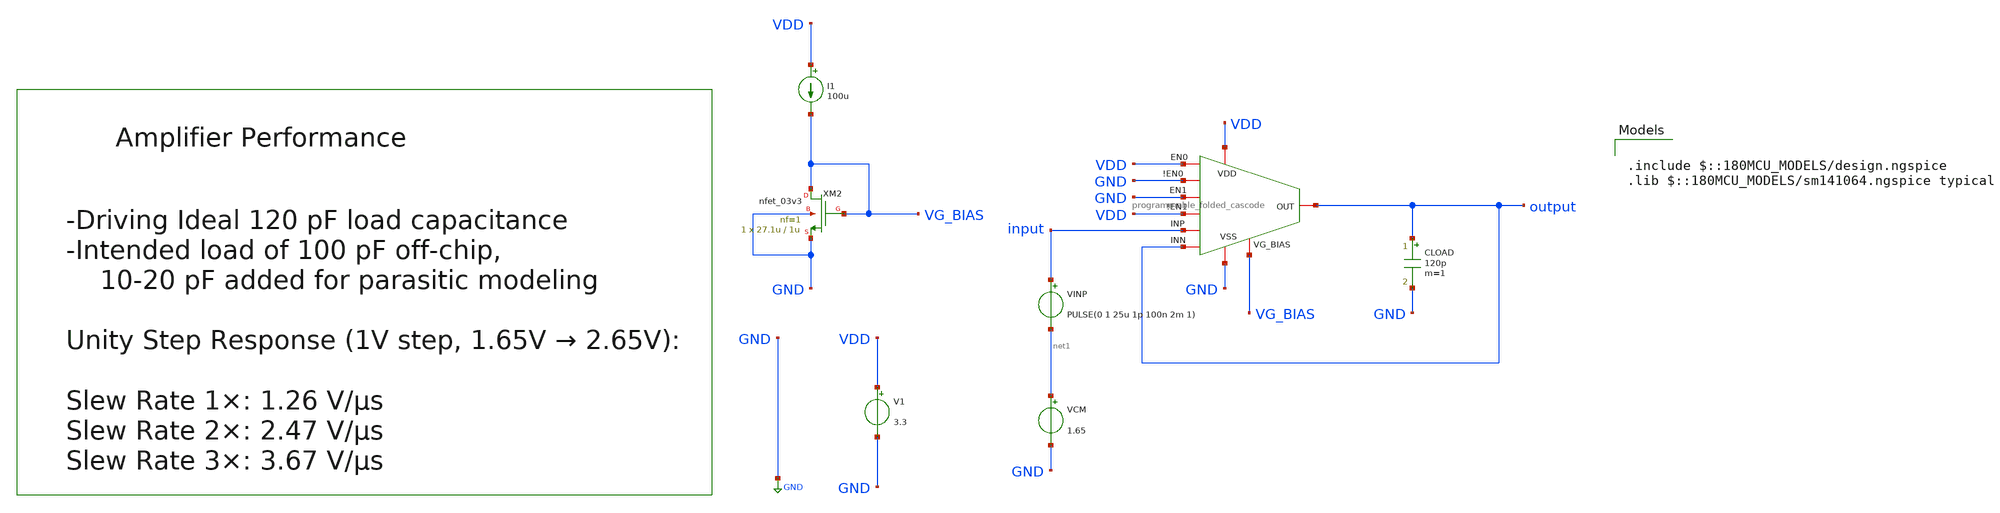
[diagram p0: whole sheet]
** sch_path: designs/libs/core_amps/ota_folded_cascode/prgram_tb/unity_step_tran_SR_tb.sch
**.subckt unity_step_tran_SR_tb
CLOAD output GND 120p m=1
VINP input net1 PULSE(0 1 25u 1p 100n 2m 1)
VCM net1 GND 1.65
x1 VDD VDD GND GND GND VDD output input output VG_BIAS programmable_folded_cascode
XM2 VG_BIAS VG_BIAS GND GND nfet_03v3 L=1u W=27.1u nf=1 ad='int((nf+1)/2) * W/nf * 0.18u' as='int((nf+2)/2) * W/nf * 0.18u'
+ pd='2*int((nf+1)/2) * (W/nf + 0.18u)' ps='2*int((nf+2)/2) * (W/nf + 0.18u)' nrd='0.18u / W' nrs='0.18u / W'
+ sa=0 sb=0 sd=0 m=1
I1 VDD VG_BIAS 100u
V1 VDD GND 3.3
**** begin user architecture code

.include $::180MCU_MODELS/design.ngspice
.lib $::180MCU_MODELS/sm141064.ngspice typical



.control
tran 1n 100u
meas tran v_before find v(output) at=24u
meas tran v_after find v(output) at=90u
let v_20 = v_before + 0.2 * (v_after - v_before)
let v_80 = v_before + 0.8 * (v_after - v_before)
meas tran t_20 when v(output) = v_20 rise = 1 from = 25u
meas tran t_80 when v(output) = v_80 rise = 1 from = 25u
let slew_rate = (v_80 - v_20) / (t_80 - t_20)
print v_before v_after
print slew_rate

plot v(input) v(output)
.endc



**** end user architecture code
**.ends

* expanding   symbol:  libs/core_amps/ota_folded_cascode/prgrm_schem/programmable_folded_cascode.sym
*+ # of pins=10
** sym_path: designs/libs/core_amps/ota_folded_cascode/prgrm_schem/programmable_folded_cascode.sym
** sch_path: designs/libs/core_amps/ota_folded_cascode/prgrm_schem/programmable_folded_cascode.sch
.subckt programmable_folded_cascode EN0 VDD !EN0 VSS EN1 !EN1 INN INP OUT VG_BIAS
*.iopin OUT
*.iopin VSS
*.iopin VDD
*.iopin EN0
*.iopin !EN0
*.iopin EN1
*.iopin !EN1
*.iopin INN
*.iopin INP
*.iopin VG_BIAS
XM29 net7 net7 VDD VDD pfet_03v3 L=1u W=23u nf=1 ad='int((nf+1)/2) * W/nf * 0.18u' as='int((nf+2)/2) * W/nf * 0.18u'
+ pd='2*int((nf+1)/2) * (W/nf + 0.18u)' ps='2*int((nf+2)/2) * (W/nf + 0.18u)' nrd='0.18u / W' nrs='0.18u / W'
+ sa=0 sb=0 sd=0 m=5
XM30 VBP2 VBP2 net7 VDD pfet_03v3 L=.5u W=19.6u nf=1 ad='int((nf+1)/2) * W/nf * 0.18u' as='int((nf+2)/2) * W/nf * 0.18u'
+ pd='2*int((nf+1)/2) * (W/nf + 0.18u)' ps='2*int((nf+2)/2) * (W/nf + 0.18u)' nrd='0.18u / W' nrs='0.18u / W'
+ sa=0 sb=0 sd=0 m=10
XM31 VBP2 VG_BIAS VSS VSS nfet_03v3 L=1u W=27.1u nf=1 ad='int((nf+1)/2) * W/nf * 0.18u' as='int((nf+2)/2) * W/nf * 0.18u'
+ pd='2*int((nf+1)/2) * (W/nf + 0.18u)' ps='2*int((nf+2)/2) * (W/nf + 0.18u)' nrd='0.18u / W' nrs='0.18u / W'
+ sa=0 sb=0 sd=0 m=1
XM32 VBN1 VBN1 VSS VSS nfet_03v3 L=1u W=27.1u nf=1 ad='int((nf+1)/2) * W/nf * 0.18u' as='int((nf+2)/2) * W/nf * 0.18u'
+ pd='2*int((nf+1)/2) * (W/nf + 0.18u)' ps='2*int((nf+2)/2) * (W/nf + 0.18u)' nrd='0.18u / W' nrs='0.18u / W'
+ sa=0 sb=0 sd=0 m=1
XM33 VBN1 net7 VDD VDD pfet_03v3 L=1u W=23u nf=1 ad='int((nf+1)/2) * W/nf * 0.18u' as='int((nf+2)/2) * W/nf * 0.18u'
+ pd='2*int((nf+1)/2) * (W/nf + 0.18u)' ps='2*int((nf+2)/2) * (W/nf + 0.18u)' nrd='0.18u / W' nrs='0.18u / W'
+ sa=0 sb=0 sd=0 m=5
XM34 VBP1 VBP1 VDD VDD pfet_03v3 L=1u W=23u nf=1 ad='int((nf+1)/2) * W/nf * 0.18u' as='int((nf+2)/2) * W/nf * 0.18u'
+ pd='2*int((nf+1)/2) * (W/nf + 0.18u)' ps='2*int((nf+2)/2) * (W/nf + 0.18u)' nrd='0.18u / W' nrs='0.18u / W'
+ sa=0 sb=0 sd=0 m=5
XM35 VBP1 VG_BIAS VSS VSS nfet_03v3 L=1u W=27.1u nf=1 ad='int((nf+1)/2) * W/nf * 0.18u' as='int((nf+2)/2) * W/nf * 0.18u'
+ pd='2*int((nf+1)/2) * (W/nf + 0.18u)' ps='2*int((nf+2)/2) * (W/nf + 0.18u)' nrd='0.18u / W' nrs='0.18u / W'
+ sa=0 sb=0 sd=0 m=1
x1 net1 VSS VBN1 VSS !EN0 VDD !EN1 EN0 EN1 VSS programmable_nfet width=20u length=1u nf=1 mult=2
x2 net2 VSS INN net1 !EN0 VDD !EN1 EN0 EN1 VSS programmable_nfet width=30u length=0.5u nf=1 mult=2
x3 net3 VSS INP net1 !EN0 VDD !EN1 EN0 EN1 VSS programmable_nfet width=30u length=0.5u nf=1 mult=2
x4 net5 VSS net5 VSS !EN0 VDD !EN1 EN0 EN1 VSS programmable_nfet width=20.5u length=1u nf=1 mult=1
x5 net6 VSS net5 VSS !EN0 VDD !EN1 EN0 EN1 VSS programmable_nfet width=20.5u length=1u nf=1 mult=1
x6 net4 VSS net4 net5 !EN0 VDD !EN1 EN0 EN1 VSS programmable_nfet width=10.5u length=0.5u nf=1
+ mult=1
x7 OUT VSS net4 net6 !EN0 VDD !EN1 EN0 EN1 VSS programmable_nfet width=10.5u length=0.5u nf=1 mult=1
x8 net4 VDD VBP2 net3 !EN0 VDD !EN1 EN0 EN1 VSS programmable_pfet width=29.6u length=0.5u nf=1
+ mult=5
x9 OUT VDD VBP2 net2 !EN0 VDD !EN1 EN0 EN1 VSS programmable_pfet width=29.6u length=0.5u nf=1 mult=5
x10 net3 VDD VBP1 VDD !EN0 VDD !EN1 EN0 EN1 VSS programmable_pfet width=34.8u length=1u nf=1 mult=10
x11 net2 VDD VBP1 VDD !EN0 VDD !EN1 EN0 EN1 VSS programmable_pfet width=34.8u length=1u nf=1 mult=10
.ends


* expanding   symbol:  libs/core_digital/schem/programmable_nfet.sym # of pins=10
** sym_path: designs/libs/core_digital/schem/programmable_nfet.sym
** sch_path: designs/libs/core_digital/schem/programmable_nfet.sch
.subckt programmable_nfet d b g s ena_bar<0> VDD ena_bar<1> ena<0> ena<1> VSS  width=0.22u
+ length=0.28u nf=1 mult=1
*.ipin VSS
*.ipin VDD
*.ipin g
*.ipin ena_bar<1>
*.ipin ena_bar<0>
*.ipin ena<1>
*.ipin ena<0>
*.iopin d
*.iopin s
*.ipin b
XM1 d net2 s b nfet_03v3 L={length} W={width} nf={nf} ad='int((nf+1)/2) * W/nf * 0.18u' as='int((nf+2)/2) * W/nf * 0.18u'
+ pd='2*int((nf+1)/2) * (W/nf + 0.18u)' ps='2*int((nf+2)/2) * (W/nf + 0.18u)' nrd='0.18u / W' nrs='0.18u / W'
+ sa=0 sb=0 sd=0 m={mult}
XM3 d net1 s b nfet_03v3 L={length} W={2*width} nf={2*nf} ad='int((nf+1)/2) * W/nf * 0.18u' as='int((nf+2)/2) * W/nf * 0.18u'
+ pd='2*int((nf+1)/2) * (W/nf + 0.18u)' ps='2*int((nf+2)/2) * (W/nf + 0.18u)' nrd='0.18u / W' nrs='0.18u / W'
+ sa=0 sb=0 sd=0 m={mult}
XM2 net1 ena_bar<1> VSS VSS nfet_03v3 L=0.28u W=0.22u nf=1 ad='int((nf+1)/2) * W/nf * 0.18u' as='int((nf+2)/2) * W/nf * 0.18u'
+ pd='2*int((nf+1)/2) * (W/nf + 0.18u)' ps='2*int((nf+2)/2) * (W/nf + 0.18u)' nrd='0.18u / W' nrs='0.18u / W'
+ sa=0 sb=0 sd=0 m=1
XM4 net2 ena_bar<0> VSS VSS nfet_03v3 L=0.28u W=0.22u nf=1 ad='int((nf+1)/2) * W/nf * 0.18u' as='int((nf+2)/2) * W/nf * 0.18u'
+ pd='2*int((nf+1)/2) * (W/nf + 0.18u)' ps='2*int((nf+2)/2) * (W/nf + 0.18u)' nrd='0.18u / W' nrs='0.18u / W'
+ sa=0 sb=0 sd=0 m=1
x1 ena_bar<0> VDD net2 g VSS ena<0> transmission_gate
x2 ena_bar<1> VDD net1 g VSS ena<1> transmission_gate
.ends


* expanding   symbol:  libs/core_digital/schem/programmable_pfet.sym # of pins=10
** sym_path: designs/libs/core_digital/schem/programmable_pfet.sym
** sch_path: designs/libs/core_digital/schem/programmable_pfet.sch
.subckt programmable_pfet d b g s ena_bar<0> VDD ena_bar<1> ena<0> ena<1> VSS  width=0.22u
+ length=0.28u nf=1 mult=1
*.ipin VSS
*.ipin VDD
*.ipin g
*.ipin ena_bar<1>
*.ipin ena_bar<0>
*.ipin ena<0>
*.iopin s
*.iopin d
*.ipin b
*.ipin ena<1>
XM1 d net2 s b pfet_03v3 L={length} W={width} nf={nf} ad='int((nf+1)/2) * W/nf * 0.18u' as='int((nf+2)/2) * W/nf * 0.18u'
+ pd='2*int((nf+1)/2) * (W/nf + 0.18u)' ps='2*int((nf+2)/2) * (W/nf + 0.18u)' nrd='0.18u / W' nrs='0.18u / W'
+ sa=0 sb=0 sd=0 m={mult}
XM3 d net1 s b pfet_03v3 L={length} W={2*width} nf={2*nf} ad='int((nf+1)/2) * W/nf * 0.18u' as='int((nf+2)/2) * W/nf * 0.18u'
+ pd='2*int((nf+1)/2) * (W/nf + 0.18u)' ps='2*int((nf+2)/2) * (W/nf + 0.18u)' nrd='0.18u / W' nrs='0.18u / W'
+ sa=0 sb=0 sd=0 m={mult}
XM2 net1 ena<1> VDD VDD pfet_03v3 L=0.28u W=0.22u nf=1 ad='int((nf+1)/2) * W/nf * 0.18u' as='int((nf+2)/2) * W/nf * 0.18u'
+ pd='2*int((nf+1)/2) * (W/nf + 0.18u)' ps='2*int((nf+2)/2) * (W/nf + 0.18u)' nrd='0.18u / W' nrs='0.18u / W'
+ sa=0 sb=0 sd=0 m=1
XM4 net2 ena<0> VDD VDD pfet_03v3 L=0.28u W=0.22u nf=1 ad='int((nf+1)/2) * W/nf * 0.18u' as='int((nf+2)/2) * W/nf * 0.18u'
+ pd='2*int((nf+1)/2) * (W/nf + 0.18u)' ps='2*int((nf+2)/2) * (W/nf + 0.18u)' nrd='0.18u / W' nrs='0.18u / W'
+ sa=0 sb=0 sd=0 m=1
x1 ena_bar<0> VDD net2 g VSS ena<0> transmission_gate
x2 ena_bar<1> VDD net1 g VSS ena<1> transmission_gate
.ends


* expanding   symbol:  libs/core_digital/schem/transmission_gate.sym # of pins=6
** sym_path: designs/libs/core_digital/schem/transmission_gate.sym
** sch_path: designs/libs/core_digital/schem/transmission_gate.sch
.subckt transmission_gate ena_bar VDD out in VSS ena
*.ipin in
*.ipin ena_bar
*.ipin ena
*.ipin VSS
*.ipin VDD
*.opin out
XM1 in ena_bar out VDD pfet_03v3 L=0.28u W=0.22u nf=1 ad='int((nf+1)/2) * W/nf * 0.18u' as='int((nf+2)/2) * W/nf * 0.18u'
+ pd='2*int((nf+1)/2) * (W/nf + 0.18u)' ps='2*int((nf+2)/2) * (W/nf + 0.18u)' nrd='0.18u / W' nrs='0.18u / W'
+ sa=0 sb=0 sd=0 m=1
XM2 in ena out VSS nfet_03v3 L=0.28u W=0.22u nf=1 ad='int((nf+1)/2) * W/nf * 0.18u' as='int((nf+2)/2) * W/nf * 0.18u'
+ pd='2*int((nf+1)/2) * (W/nf + 0.18u)' ps='2*int((nf+2)/2) * (W/nf + 0.18u)' nrd='0.18u / W' nrs='0.18u / W'
+ sa=0 sb=0 sd=0 m=1
.ends

.GLOBAL GND
.end
